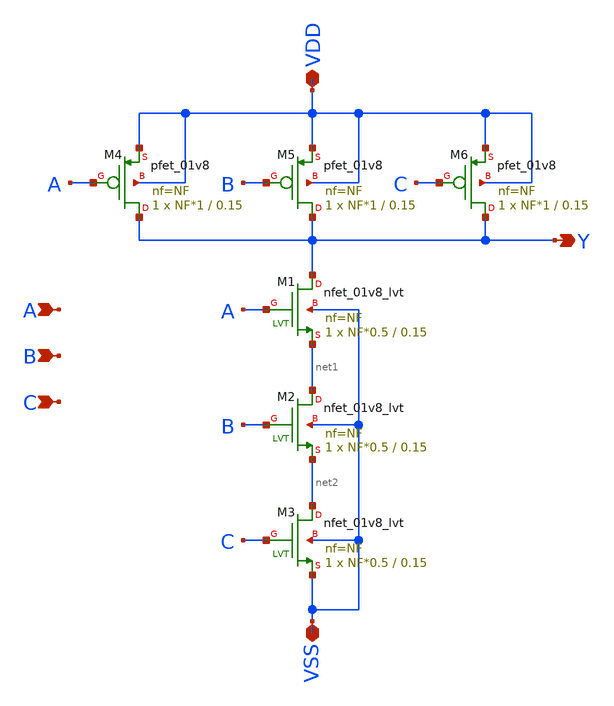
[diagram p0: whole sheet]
** sch_path: xschem_lib/DFFRAM_full_custom/nand_3in.sch
**.subckt nand_3in VDD Y VSS A B C
*.iopin VDD
*.opin Y
*.iopin VSS
*.ipin A
*.ipin B
*.ipin C
XM1 Y A net1 VSS sky130_fd_pr__nfet_01v8_lvt L=0.15 W=NF*0.5 nf=NF ad='int((nf+1)/2) * W/nf * 0.29' as='int((nf+2)/2) * W/nf * 0.29'
+ pd='2*int((nf+1)/2) * (W/nf + 0.29)' ps='2*int((nf+2)/2) * (W/nf + 0.29)' nrd='0.29 / W' nrs='0.29 / W'
+ sa=0 sb=0 sd=0 mult=1 m=1
XM4 Y A VDD VDD sky130_fd_pr__pfet_01v8 L=0.15 W=NF*1 nf=NF ad='int((nf+1)/2) * W/nf * 0.29' as='int((nf+2)/2) * W/nf * 0.29'
+ pd='2*int((nf+1)/2) * (W/nf + 0.29)' ps='2*int((nf+2)/2) * (W/nf + 0.29)' nrd='0.29 / W' nrs='0.29 / W'
+ sa=0 sb=0 sd=0 mult=1 m=1
XM2 net1 B net2 VSS sky130_fd_pr__nfet_01v8_lvt L=0.15 W=NF*0.5 nf=NF ad='int((nf+1)/2) * W/nf * 0.29'
+ as='int((nf+2)/2) * W/nf * 0.29' pd='2*int((nf+1)/2) * (W/nf + 0.29)' ps='2*int((nf+2)/2) * (W/nf + 0.29)'
+ nrd='0.29 / W' nrs='0.29 / W' sa=0 sb=0 sd=0 mult=1 m=1
XM3 net2 C VSS VSS sky130_fd_pr__nfet_01v8_lvt L=0.15 W=NF*0.5 nf=NF ad='int((nf+1)/2) * W/nf * 0.29'
+ as='int((nf+2)/2) * W/nf * 0.29' pd='2*int((nf+1)/2) * (W/nf + 0.29)' ps='2*int((nf+2)/2) * (W/nf + 0.29)'
+ nrd='0.29 / W' nrs='0.29 / W' sa=0 sb=0 sd=0 mult=1 m=1
XM5 Y B VDD VDD sky130_fd_pr__pfet_01v8 L=0.15 W=NF*1 nf=NF ad='int((nf+1)/2) * W/nf * 0.29' as='int((nf+2)/2) * W/nf * 0.29'
+ pd='2*int((nf+1)/2) * (W/nf + 0.29)' ps='2*int((nf+2)/2) * (W/nf + 0.29)' nrd='0.29 / W' nrs='0.29 / W'
+ sa=0 sb=0 sd=0 mult=1 m=1
XM6 Y C VDD VDD sky130_fd_pr__pfet_01v8 L=0.15 W=NF*1 nf=NF ad='int((nf+1)/2) * W/nf * 0.29' as='int((nf+2)/2) * W/nf * 0.29'
+ pd='2*int((nf+1)/2) * (W/nf + 0.29)' ps='2*int((nf+2)/2) * (W/nf + 0.29)' nrd='0.29 / W' nrs='0.29 / W'
+ sa=0 sb=0 sd=0 mult=1 m=1
**.ends
.end
